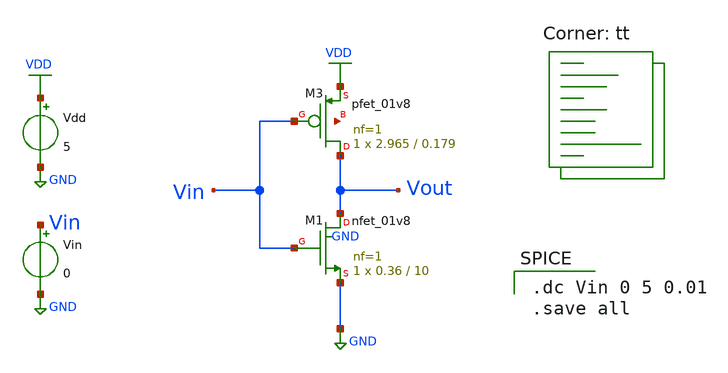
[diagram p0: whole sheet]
** sch_path: vdd1.8V/inverter_sat_14.sch
**.subckt inverter_sat_14
Vdd VDD GND 5
XM1 Vout Vin GND GND sky130_fd_pr__nfet_01v8 L=10 W=0.36 nf=1 ad='int((nf+1)/2) * W/nf * 0.29' as='int((nf+2)/2) * W/nf * 0.29'
+ pd='2*int((nf+1)/2) * (W/nf + 0.29)' ps='2*int((nf+2)/2) * (W/nf + 0.29)' nrd='0.29 / W' nrs='0.29 / W'
+ sa=0 sb=0 sd=0 mult=1 m=1
Vin Vin GND 0
XM3 Vout Vin VDD net1 sky130_fd_pr__pfet_01v8 L=0.179 W=2.965 nf=1 ad='int((nf+1)/2) * W/nf * 0.29' as='int((nf+2)/2) * W/nf * 0.29'
+ pd='2*int((nf+1)/2) * (W/nf + 0.29)' ps='2*int((nf+2)/2) * (W/nf + 0.29)' nrd='0.29 / W' nrs='0.29 / W'
+ sa=0 sb=0 sd=0 mult=1 m=1
**** begin user architecture code

.dc Vin 0 5 0.01
.save all

.lib $::SKYWATER_MODELS/sky130.lib.spice tt
**** end user architecture code
**.ends
.GLOBAL GND
.GLOBAL VDD
.end
